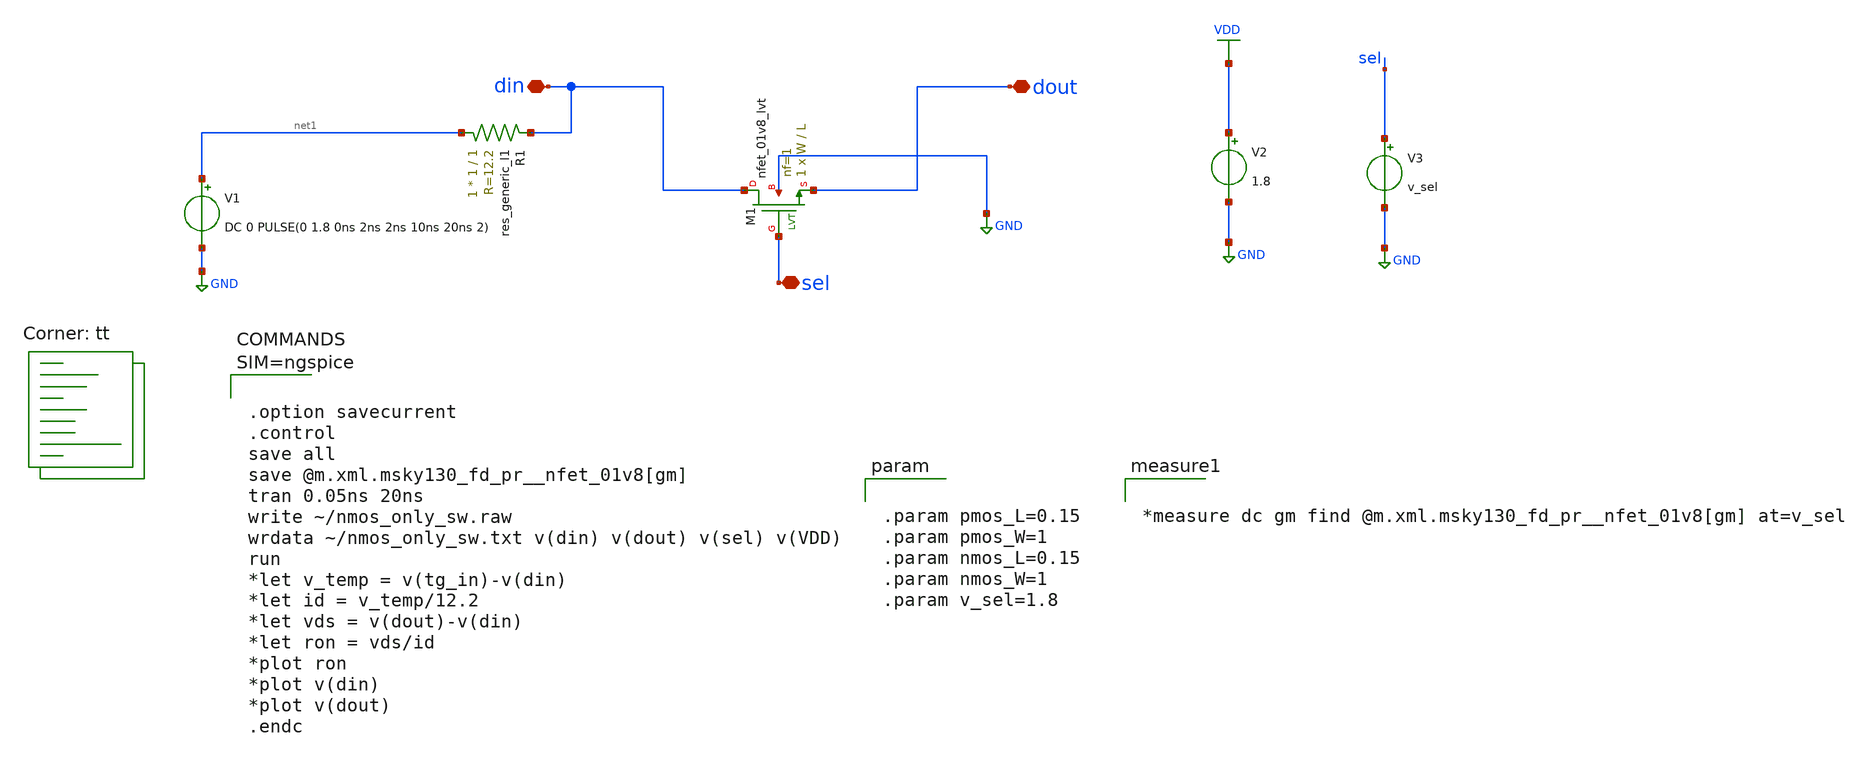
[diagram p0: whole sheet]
** sch_path: tseng_workspace/transmission_gate/schematic/spice/nmos_only_sw.sch
**.subckt nmos_only_sw din dout sel
*.iopin din
*.iopin dout
*.iopin sel
V2 VDD GND 1.8
V3 sel GND v_sel
R1 net1 din sky130_fd_pr__res_generic_l1 W=1 L=1 m=1
V1 net1 GND DC 0 PULSE(0 1.8 0ns 2ns 2ns 10ns 20ns 2)
XM1 din sel dout GND sky130_fd_pr__nfet_01v8_lvt L=L W=W nf=1 ad='int((1 + 1)/2) * W / 1 * 0.29' as='int((1 + 2)/2) * W / 1 * 0.29'
+ pd='2*int((1 + 1)/2) * (W / 1 + 0.29)' ps='2*int((1 + 2)/2) * (W / 1 + 0.29)' nrd='0.29 / W ' nrs='0.29 / W '
+ sa=0 sb=0 sd=0 mult=1 m=1
**** begin user architecture code



.option savecurrent
.control
save all
save @m.xml.msky130_fd_pr__nfet_01v8[gm]
tran 0.05ns 20ns
write ~/nmos_only_sw.raw
wrdata ~/nmos_only_sw.txt v(din) v(dout) v(sel) v(VDD)
run
*let v_temp = v(tg_in)-v(din)
*let id = v_temp/12.2
*let vds = v(dout)-v(din)
*let ron = vds/id
*plot ron
*plot v(din)
*plot v(dout)
.endc




.param pmos_L=0.15
.param pmos_W=1
.param nmos_L=0.15
.param nmos_W=1
.param v_sel=1.8


*measure dc gm find @m.xml.msky130_fd_pr__nfet_01v8[gm] at=v_sel

.lib $::SKYWATER_MODELS/sky130.lib.spice tt
**** end user architecture code
**.ends
.GLOBAL GND
.GLOBAL VDD
.end
